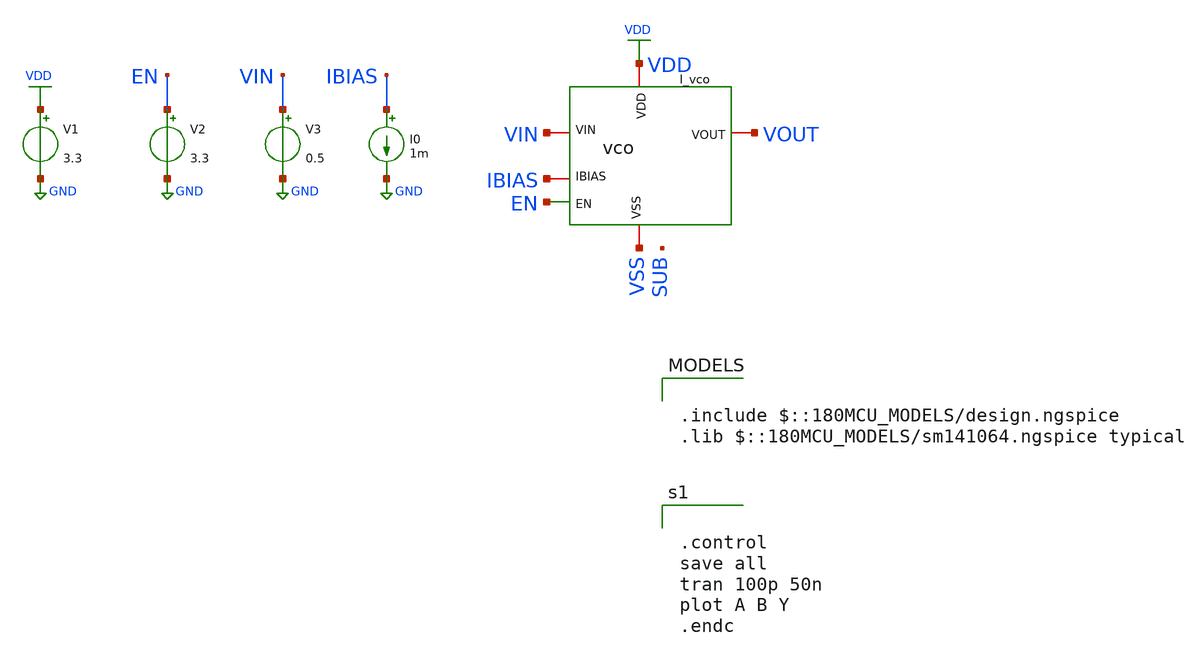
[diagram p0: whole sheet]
** sch_path: designs/libs/tb_vco/tb_vco/tb_vco.sch
**.subckt tb_vco
I_vco VDD IBIAS VOUT EN VSS VIN vco
V1 VDD GND 3.3
V2 EN GND 3.3
V3 VIN GND 0.5
I0 IBIAS GND 1m
**** begin user architecture code

.include $::180MCU_MODELS/design.ngspice
.lib $::180MCU_MODELS/sm141064.ngspice typical



.control
save all
tran 100p 50n
plot A B Y
.endc


**** end user architecture code
**.ends
.GLOBAL GND
.GLOBAL VDD
.end
